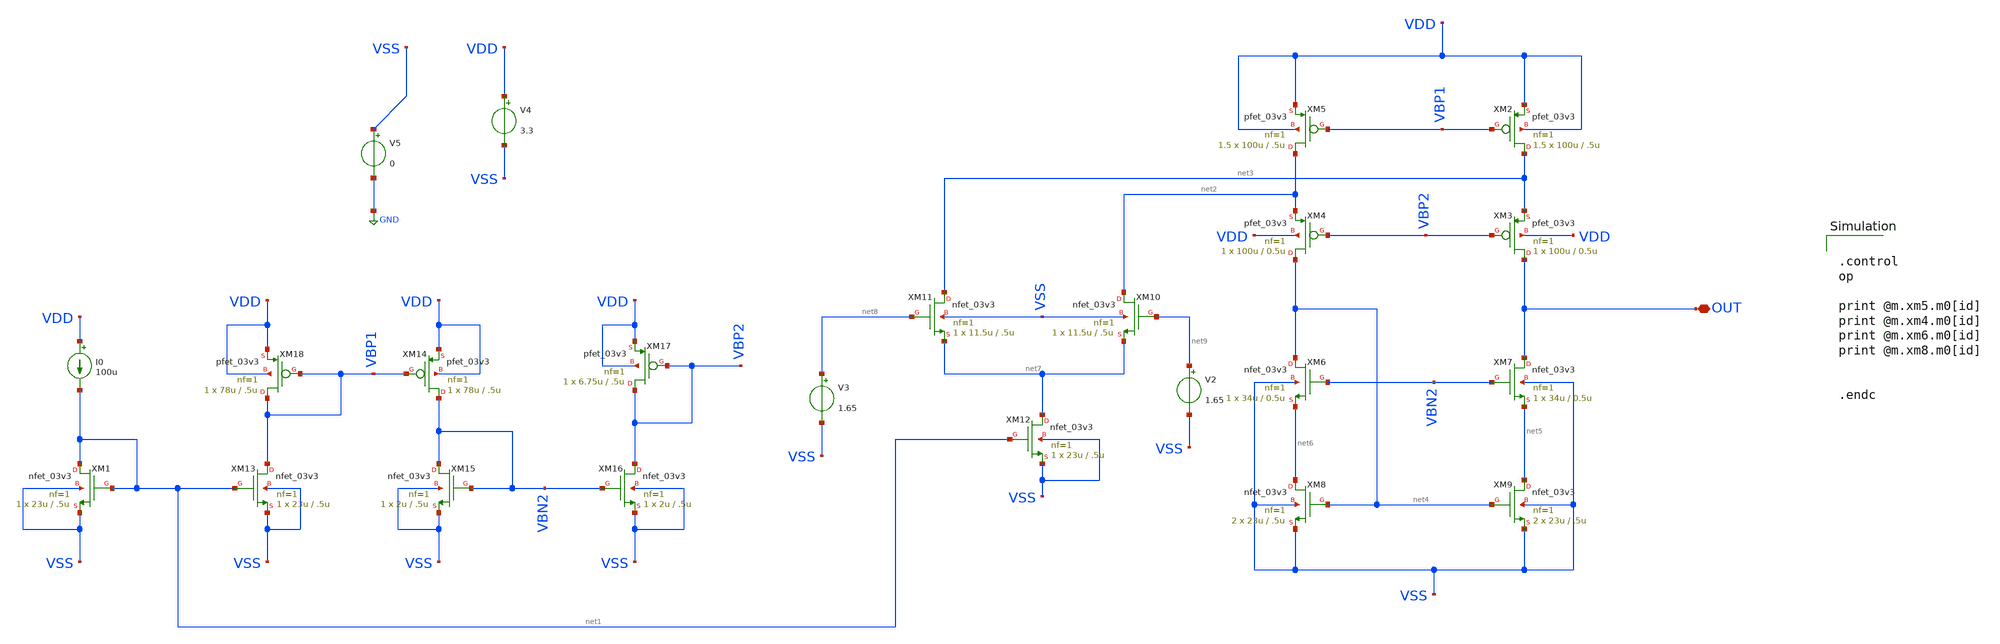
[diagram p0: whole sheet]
** sch_path: designs/libs/tb_amps/tb_ota_folded_cascode/sizing_helper.sch
**.subckt sizing_helper OUT
*.iopin OUT
XM1 net1 net1 VSS VSS nfet_03v3 L=.5u W=23u nf=1 ad='int((nf+1)/2) * W/nf * 0.18u' as='int((nf+2)/2) * W/nf * 0.18u'
+ pd='2*int((nf+1)/2) * (W/nf + 0.18u)' ps='2*int((nf+2)/2) * (W/nf + 0.18u)' nrd='0.18u / W' nrs='0.18u / W'
+ sa=0 sb=0 sd=0 m=1
XM2 net3 VBP1 VDD VDD pfet_03v3 L=.5u W=100u nf=1 ad='int((nf+1)/2) * W/nf * 0.18u' as='int((nf+2)/2) * W/nf * 0.18u'
+ pd='2*int((nf+1)/2) * (W/nf + 0.18u)' ps='2*int((nf+2)/2) * (W/nf + 0.18u)' nrd='0.18u / W' nrs='0.18u / W'
+ sa=0 sb=0 sd=0 m=1.5
XM3 OUT VBP2 net3 VDD pfet_03v3 L=0.5u W=100u nf=1 ad='int((nf+1)/2) * W/nf * 0.18u' as='int((nf+2)/2) * W/nf * 0.18u'
+ pd='2*int((nf+1)/2) * (W/nf + 0.18u)' ps='2*int((nf+2)/2) * (W/nf + 0.18u)' nrd='0.18u / W' nrs='0.18u / W'
+ sa=0 sb=0 sd=0 m=1
XM4 net4 VBP2 net2 VDD pfet_03v3 L=0.5u W=100u nf=1 ad='int((nf+1)/2) * W/nf * 0.18u' as='int((nf+2)/2) * W/nf * 0.18u'
+ pd='2*int((nf+1)/2) * (W/nf + 0.18u)' ps='2*int((nf+2)/2) * (W/nf + 0.18u)' nrd='0.18u / W' nrs='0.18u / W'
+ sa=0 sb=0 sd=0 m=1
XM5 net2 VBP1 VDD VDD pfet_03v3 L=.5u W=100u nf=1 ad='int((nf+1)/2) * W/nf * 0.18u' as='int((nf+2)/2) * W/nf * 0.18u'
+ pd='2*int((nf+1)/2) * (W/nf + 0.18u)' ps='2*int((nf+2)/2) * (W/nf + 0.18u)' nrd='0.18u / W' nrs='0.18u / W'
+ sa=0 sb=0 sd=0 m=1.5
XM6 net4 VBN2 net6 VSS nfet_03v3 L=0.5u W=34u nf=1 ad='int((nf+1)/2) * W/nf * 0.18u' as='int((nf+2)/2) * W/nf * 0.18u'
+ pd='2*int((nf+1)/2) * (W/nf + 0.18u)' ps='2*int((nf+2)/2) * (W/nf + 0.18u)' nrd='0.18u / W' nrs='0.18u / W'
+ sa=0 sb=0 sd=0 m=1
XM7 OUT VBN2 net5 VSS nfet_03v3 L=0.5u W=34u nf=1 ad='int((nf+1)/2) * W/nf * 0.18u' as='int((nf+2)/2) * W/nf * 0.18u'
+ pd='2*int((nf+1)/2) * (W/nf + 0.18u)' ps='2*int((nf+2)/2) * (W/nf + 0.18u)' nrd='0.18u / W' nrs='0.18u / W'
+ sa=0 sb=0 sd=0 m=1
XM8 net6 net4 VSS VSS nfet_03v3 L=.5u W=23u nf=1 ad='int((nf+1)/2) * W/nf * 0.18u' as='int((nf+2)/2) * W/nf * 0.18u'
+ pd='2*int((nf+1)/2) * (W/nf + 0.18u)' ps='2*int((nf+2)/2) * (W/nf + 0.18u)' nrd='0.18u / W' nrs='0.18u / W'
+ sa=0 sb=0 sd=0 m=2
XM9 net5 net4 VSS VSS nfet_03v3 L=.5u W=23u nf=1 ad='int((nf+1)/2) * W/nf * 0.18u' as='int((nf+2)/2) * W/nf * 0.18u'
+ pd='2*int((nf+1)/2) * (W/nf + 0.18u)' ps='2*int((nf+2)/2) * (W/nf + 0.18u)' nrd='0.18u / W' nrs='0.18u / W'
+ sa=0 sb=0 sd=0 m=2
XM10 net2 net9 net7 VSS nfet_03v3 L=.5u W=11.5u nf=1 ad='int((nf+1)/2) * W/nf * 0.18u' as='int((nf+2)/2) * W/nf * 0.18u'
+ pd='2*int((nf+1)/2) * (W/nf + 0.18u)' ps='2*int((nf+2)/2) * (W/nf + 0.18u)' nrd='0.18u / W' nrs='0.18u / W'
+ sa=0 sb=0 sd=0 m=1
XM12 net7 net1 VSS VSS nfet_03v3 L=.5u W=23u nf=1 ad='int((nf+1)/2) * W/nf * 0.18u' as='int((nf+2)/2) * W/nf * 0.18u'
+ pd='2*int((nf+1)/2) * (W/nf + 0.18u)' ps='2*int((nf+2)/2) * (W/nf + 0.18u)' nrd='0.18u / W' nrs='0.18u / W'
+ sa=0 sb=0 sd=0 m=1
XM18 VBP1 VBP1 VDD VDD pfet_03v3 L=.5u W=78u nf=1 ad='int((nf+1)/2) * W/nf * 0.18u' as='int((nf+2)/2) * W/nf * 0.18u'
+ pd='2*int((nf+1)/2) * (W/nf + 0.18u)' ps='2*int((nf+2)/2) * (W/nf + 0.18u)' nrd='0.18u / W' nrs='0.18u / W'
+ sa=0 sb=0 sd=0 m=1
XM11 net3 net8 net7 VSS nfet_03v3 L=.5u W=11.5u nf=1 ad='int((nf+1)/2) * W/nf * 0.18u' as='int((nf+2)/2) * W/nf * 0.18u'
+ pd='2*int((nf+1)/2) * (W/nf + 0.18u)' ps='2*int((nf+2)/2) * (W/nf + 0.18u)' nrd='0.18u / W' nrs='0.18u / W'
+ sa=0 sb=0 sd=0 m=1
XM13 VBP1 net1 VSS VSS nfet_03v3 L=.5u W=23u nf=1 ad='int((nf+1)/2) * W/nf * 0.18u' as='int((nf+2)/2) * W/nf * 0.18u'
+ pd='2*int((nf+1)/2) * (W/nf + 0.18u)' ps='2*int((nf+2)/2) * (W/nf + 0.18u)' nrd='0.18u / W' nrs='0.18u / W'
+ sa=0 sb=0 sd=0 m=1
XM14 VBN2 VBP1 VDD VDD pfet_03v3 L=.5u W=78u nf=1 ad='int((nf+1)/2) * W/nf * 0.18u' as='int((nf+2)/2) * W/nf * 0.18u'
+ pd='2*int((nf+1)/2) * (W/nf + 0.18u)' ps='2*int((nf+2)/2) * (W/nf + 0.18u)' nrd='0.18u / W' nrs='0.18u / W'
+ sa=0 sb=0 sd=0 m=1
XM15 VBN2 VBN2 VSS VSS nfet_03v3 L=.5u W=2u nf=1 ad='int((nf+1)/2) * W/nf * 0.18u' as='int((nf+2)/2) * W/nf * 0.18u'
+ pd='2*int((nf+1)/2) * (W/nf + 0.18u)' ps='2*int((nf+2)/2) * (W/nf + 0.18u)' nrd='0.18u / W' nrs='0.18u / W'
+ sa=0 sb=0 sd=0 m=1
XM16 VBP2 VBN2 VSS VSS nfet_03v3 L=.5u W=2u nf=1 ad='int((nf+1)/2) * W/nf * 0.18u' as='int((nf+2)/2) * W/nf * 0.18u'
+ pd='2*int((nf+1)/2) * (W/nf + 0.18u)' ps='2*int((nf+2)/2) * (W/nf + 0.18u)' nrd='0.18u / W' nrs='0.18u / W'
+ sa=0 sb=0 sd=0 m=1
XM17 VBP2 VBP2 VDD VDD pfet_03v3 L=.5u W=6.75u nf=1 ad='int((nf+1)/2) * W/nf * 0.18u' as='int((nf+2)/2) * W/nf * 0.18u'
+ pd='2*int((nf+1)/2) * (W/nf + 0.18u)' ps='2*int((nf+2)/2) * (W/nf + 0.18u)' nrd='0.18u / W' nrs='0.18u / W'
+ sa=0 sb=0 sd=0 m=1
V2 net9 VSS 1.65
V3 net8 VSS 1.65
V4 VDD VSS 3.3
I0 VDD net1 100u
V5 VSS GND 0
**** begin user architecture code

.include $::180MCU_MODELS/design.ngspice
.lib $::180MCU_MODELS/sm141064.ngspice typical



.control
op

print @m.xm5.m0[id]
print @m.xm4.m0[id]
print @m.xm6.m0[id]
print @m.xm8.m0[id]


.endc


**** end user architecture code
**.ends
.GLOBAL GND
.end
